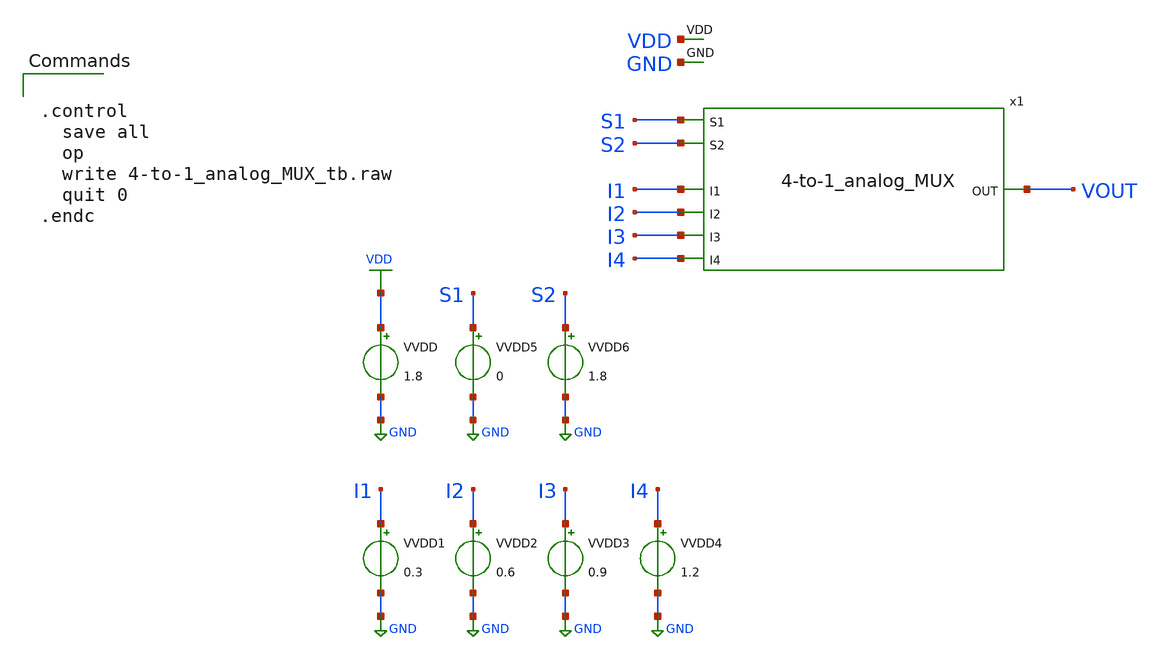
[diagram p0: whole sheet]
** sch_path: xschem/4-to-1_analog_MUX_tb.sch
**.subckt 4-to-1_analog_MUX_tb
x1 S1 S2 VDD GND I1 I2 VOUT I3 I4 4-to-1_analog_MUX
VVDD VDD GND 1.8
VVDD1 I1 GND 0.3
VVDD2 I2 GND 0.6
VVDD3 I3 GND 0.9
VVDD4 I4 GND 1.2
VVDD5 S1 GND 0
VVDD6 S2 GND 1.8
**** begin user architecture code

** opencircuitdesign pdks install
.lib $::SKYWATER_MODELS/sky130.lib.spice tt




.control
  save all
  op
  write 4-to-1_analog_MUX_tb.raw
  quit 0
.endc


**** end user architecture code
**.ends

* expanding   symbol:  4-to-1_analog_MUX.sym # of pins=9
** sym_path: xschem/4-to-1_analog_MUX.sym
** sch_path: xschem/4-to-1_analog_MUX.sch
.subckt 4-to-1_analog_MUX S1 S2 VDD GND I1 I2 OUT I3 I4
*.ipin I1
*.ipin I2
*.ipin I3
*.ipin I4
*.opin OUT
*.ipin S1
*.ipin S2
*.ipin VDD
*.ipin GND
x1 S1 S1bar GND VDD Inverter
x2 S2 S2bar GND VDD Inverter
XM9 net1 S2 OUT VDD sky130_fd_pr__pfet_01v8 L=0.5 W=1 nf=1 ad='int((nf+1)/2) * W/nf * 0.29' as='int((nf+2)/2) * W/nf * 0.29'
+ pd='2*int((nf+1)/2) * (W/nf + 0.29)' ps='2*int((nf+2)/2) * (W/nf + 0.29)' nrd='0.29 / W' nrs='0.29 / W'
+ sa=0 sb=0 sd=0 mult=1 m=1
XM1 I1 S1 net1 VDD sky130_fd_pr__pfet_01v8 L=0.5 W=1 nf=1 ad='int((nf+1)/2) * W/nf * 0.29' as='int((nf+2)/2) * W/nf * 0.29'
+ pd='2*int((nf+1)/2) * (W/nf + 0.29)' ps='2*int((nf+2)/2) * (W/nf + 0.29)' nrd='0.29 / W' nrs='0.29 / W'
+ sa=0 sb=0 sd=0 mult=1 m=1
XM2 I3 S1bar net1 VDD sky130_fd_pr__pfet_01v8 L=0.5 W=1 nf=1 ad='int((nf+1)/2) * W/nf * 0.29' as='int((nf+2)/2) * W/nf * 0.29'
+ pd='2*int((nf+1)/2) * (W/nf + 0.29)' ps='2*int((nf+2)/2) * (W/nf + 0.29)' nrd='0.29 / W' nrs='0.29 / W'
+ sa=0 sb=0 sd=0 mult=1 m=1
XM5 I2 S1 net2 VDD sky130_fd_pr__pfet_01v8 L=0.5 W=1 nf=1 ad='int((nf+1)/2) * W/nf * 0.29' as='int((nf+2)/2) * W/nf * 0.29'
+ pd='2*int((nf+1)/2) * (W/nf + 0.29)' ps='2*int((nf+2)/2) * (W/nf + 0.29)' nrd='0.29 / W' nrs='0.29 / W'
+ sa=0 sb=0 sd=0 mult=1 m=1
XM7 I4 S1bar net2 VDD sky130_fd_pr__pfet_01v8 L=0.5 W=1 nf=1 ad='int((nf+1)/2) * W/nf * 0.29' as='int((nf+2)/2) * W/nf * 0.29'
+ pd='2*int((nf+1)/2) * (W/nf + 0.29)' ps='2*int((nf+2)/2) * (W/nf + 0.29)' nrd='0.29 / W' nrs='0.29 / W'
+ sa=0 sb=0 sd=0 mult=1 m=1
XM11 net2 S2bar OUT VDD sky130_fd_pr__pfet_01v8 L=0.5 W=1 nf=1 ad='int((nf+1)/2) * W/nf * 0.29' as='int((nf+2)/2) * W/nf * 0.29'
+ pd='2*int((nf+1)/2) * (W/nf + 0.29)' ps='2*int((nf+2)/2) * (W/nf + 0.29)' nrd='0.29 / W' nrs='0.29 / W'
+ sa=0 sb=0 sd=0 mult=1 m=1
XM3 I1 S1bar net1 GND sky130_fd_pr__nfet_01v8 L=1 W=1 nf=1 ad='int((nf+1)/2) * W/nf * 0.29' as='int((nf+2)/2) * W/nf * 0.29'
+ pd='2*int((nf+1)/2) * (W/nf + 0.29)' ps='2*int((nf+2)/2) * (W/nf + 0.29)' nrd='0.29 / W' nrs='0.29 / W'
+ sa=0 sb=0 sd=0 mult=1 m=1
XM4 I3 S1 net1 GND sky130_fd_pr__nfet_01v8 L=1 W=1 nf=1 ad='int((nf+1)/2) * W/nf * 0.29' as='int((nf+2)/2) * W/nf * 0.29'
+ pd='2*int((nf+1)/2) * (W/nf + 0.29)' ps='2*int((nf+2)/2) * (W/nf + 0.29)' nrd='0.29 / W' nrs='0.29 / W'
+ sa=0 sb=0 sd=0 mult=1 m=1
XM10 net1 S2bar OUT GND sky130_fd_pr__nfet_01v8 L=1 W=1 nf=1 ad='int((nf+1)/2) * W/nf * 0.29' as='int((nf+2)/2) * W/nf * 0.29'
+ pd='2*int((nf+1)/2) * (W/nf + 0.29)' ps='2*int((nf+2)/2) * (W/nf + 0.29)' nrd='0.29 / W' nrs='0.29 / W'
+ sa=0 sb=0 sd=0 mult=1 m=1
XM6 I2 S1bar net2 GND sky130_fd_pr__nfet_01v8 L=1 W=1 nf=1 ad='int((nf+1)/2) * W/nf * 0.29' as='int((nf+2)/2) * W/nf * 0.29'
+ pd='2*int((nf+1)/2) * (W/nf + 0.29)' ps='2*int((nf+2)/2) * (W/nf + 0.29)' nrd='0.29 / W' nrs='0.29 / W'
+ sa=0 sb=0 sd=0 mult=1 m=1
XM8 I4 S1 net2 GND sky130_fd_pr__nfet_01v8 L=1 W=1 nf=1 ad='int((nf+1)/2) * W/nf * 0.29' as='int((nf+2)/2) * W/nf * 0.29'
+ pd='2*int((nf+1)/2) * (W/nf + 0.29)' ps='2*int((nf+2)/2) * (W/nf + 0.29)' nrd='0.29 / W' nrs='0.29 / W'
+ sa=0 sb=0 sd=0 mult=1 m=1
XM12 net2 S2 OUT GND sky130_fd_pr__nfet_01v8 L=1 W=1 nf=1 ad='int((nf+1)/2) * W/nf * 0.29' as='int((nf+2)/2) * W/nf * 0.29'
+ pd='2*int((nf+1)/2) * (W/nf + 0.29)' ps='2*int((nf+2)/2) * (W/nf + 0.29)' nrd='0.29 / W' nrs='0.29 / W'
+ sa=0 sb=0 sd=0 mult=1 m=1
.ends


* expanding   symbol:  Inverter.sym # of pins=4
** sym_path: xschem/Inverter.sym
** sch_path: xschem/Inverter.sch
.subckt Inverter Vin Vout GND VDD
*.opin Vout
*.ipin Vin
*.ipin VDD
*.ipin GND
XM1 Vout Vin VDD VDD sky130_fd_pr__pfet_01v8 L=0.5 W=1 nf=1 ad='int((nf+1)/2) * W/nf * 0.29' as='int((nf+2)/2) * W/nf * 0.29'
+ pd='2*int((nf+1)/2) * (W/nf + 0.29)' ps='2*int((nf+2)/2) * (W/nf + 0.29)' nrd='0.29 / W' nrs='0.29 / W'
+ sa=0 sb=0 sd=0 mult=1 m=1
XM2 Vout Vin GND GND sky130_fd_pr__nfet_01v8 L=1 W=1 nf=1 ad='int((nf+1)/2) * W/nf * 0.29' as='int((nf+2)/2) * W/nf * 0.29'
+ pd='2*int((nf+1)/2) * (W/nf + 0.29)' ps='2*int((nf+2)/2) * (W/nf + 0.29)' nrd='0.29 / W' nrs='0.29 / W'
+ sa=0 sb=0 sd=0 mult=1 m=1
.ends

.GLOBAL GND
.GLOBAL VDD
.end
